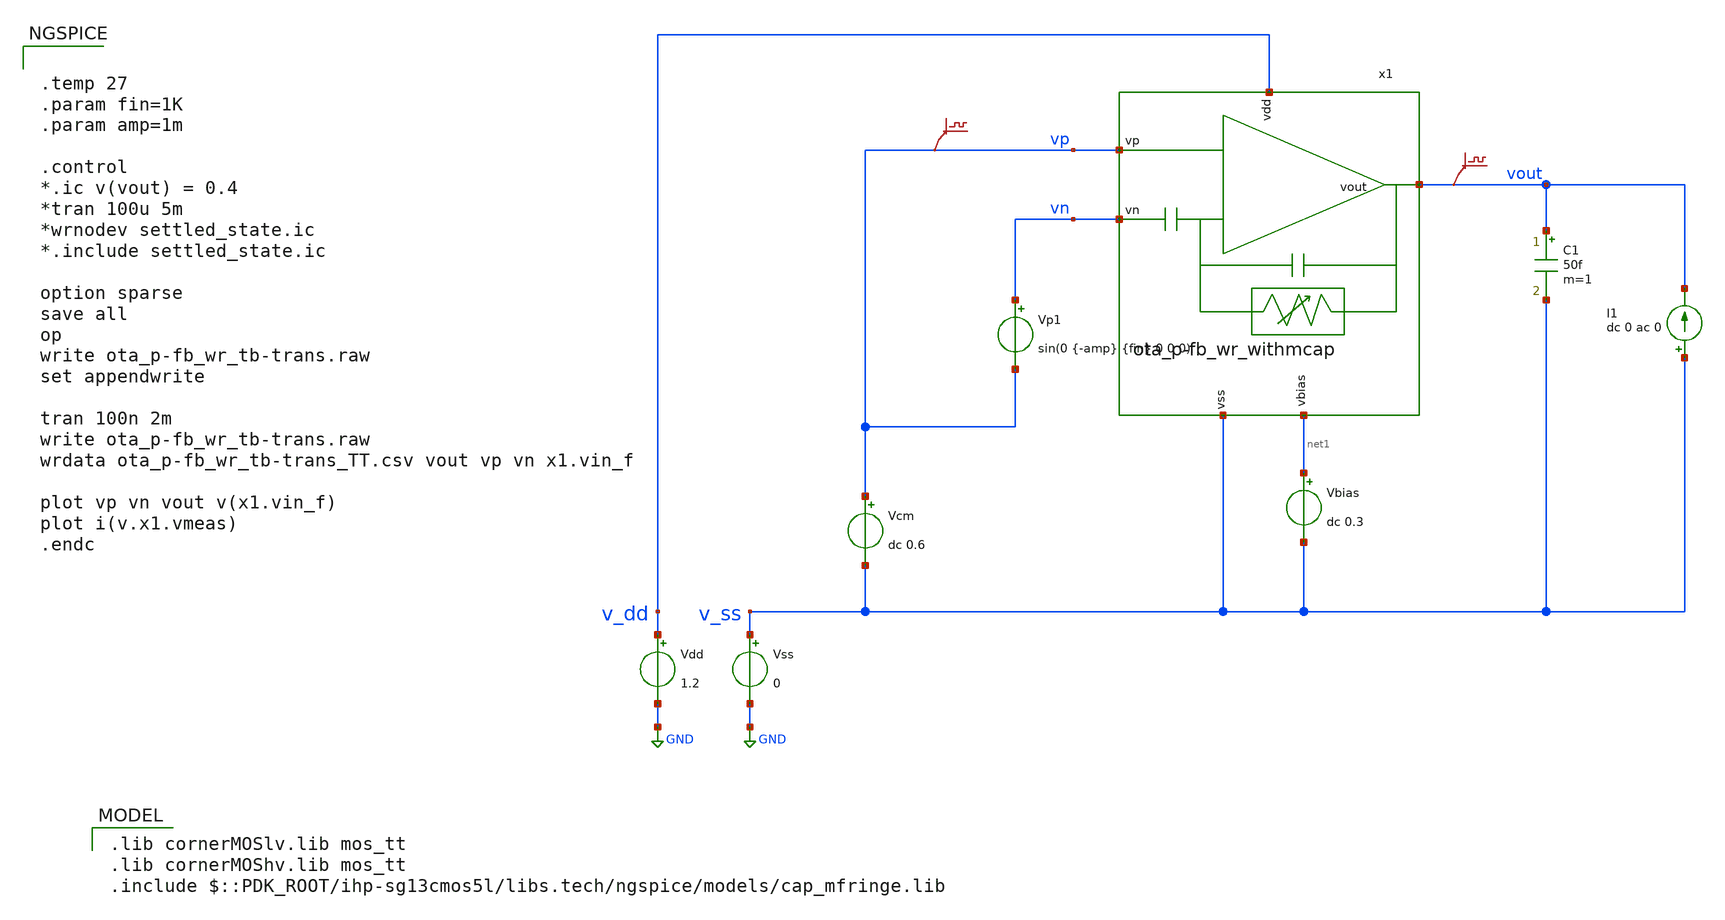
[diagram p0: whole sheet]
** sch_path: v2_feature_extr_withf/ota_p-fb-wr_tb-trans.sch
* (c) 2024-2025 Harald Pretl, Apache-2.0 license
**.subckt ota_p-fb-wr_tb-trans
Vdd v_dd GND 1.2
Vss v_ss GND 0
C1 vout v_ss 50f m=1
Vcm vp v_ss dc 0.6
.save v(vp)
.save v(vout)
I1 v_ss vout dc 0 ac 0
Vp1 vn vp sin(0 {-amp} {fin} 0 0 0)
Vbias net1 v_ss dc 0.3
x1 v_dd vp vout vn v_ss net1 ota_p-fb_wr_withmcap
**** begin user architecture code
 .lib cornerMOSlv.lib mos_tt
.lib cornerMOShv.lib mos_tt
.include $::PDK_ROOT/ihp-sg13cmos5l/libs.tech/ngspice/models/cap_mfringe.lib



.temp 27
.param fin=1K
.param amp=1m

.control
*.ic v(vout) = 0.4
*tran 100u 5m
*wrnodev settled_state.ic
*.include settled_state.ic

option sparse
save all
op
write ota_p-fb_wr_tb-trans.raw
set appendwrite

tran 100n 2m
write ota_p-fb_wr_tb-trans.raw
wrdata ota_p-fb_wr_tb-trans_TT.csv vout vp vn x1.vin_f

plot vp vn vout v(x1.vin_f)
plot i(v.x1.vmeas)
.endc


**** end user architecture code
**.ends
.GLOBAL GND
.end
